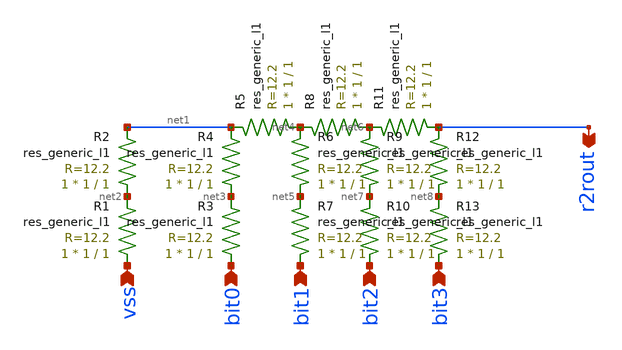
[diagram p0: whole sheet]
** sch_path: r2r.sch
**.subckt r2r r2rout vss bit0 bit1 bit2 bit3
*.opin r2rout
*.ipin vss
*.ipin bit0
*.ipin bit1
*.ipin bit2
*.ipin bit3
R1 vss net2 sky130_fd_pr__res_generic_l1 W=1 L=1 m=1
R2 net2 net1 sky130_fd_pr__res_generic_l1 W=1 L=1 m=1
R3 bit0 net3 sky130_fd_pr__res_generic_l1 W=1 L=1 m=1
R4 net3 net1 sky130_fd_pr__res_generic_l1 W=1 L=1 m=1
R5 net4 net1 sky130_fd_pr__res_generic_l1 W=1 L=1 m=1
R6 net5 net4 sky130_fd_pr__res_generic_l1 W=1 L=1 m=1
R7 bit1 net5 sky130_fd_pr__res_generic_l1 W=1 L=1 m=1
R8 net6 net4 sky130_fd_pr__res_generic_l1 W=1 L=1 m=1
R9 net7 net6 sky130_fd_pr__res_generic_l1 W=1 L=1 m=1
R10 bit2 net7 sky130_fd_pr__res_generic_l1 W=1 L=1 m=1
R11 r2rout net6 sky130_fd_pr__res_generic_l1 W=1 L=1 m=1
R12 net8 r2rout sky130_fd_pr__res_generic_l1 W=1 L=1 m=1
R13 bit3 net8 sky130_fd_pr__res_generic_l1 W=1 L=1 m=1
**.ends
.end
